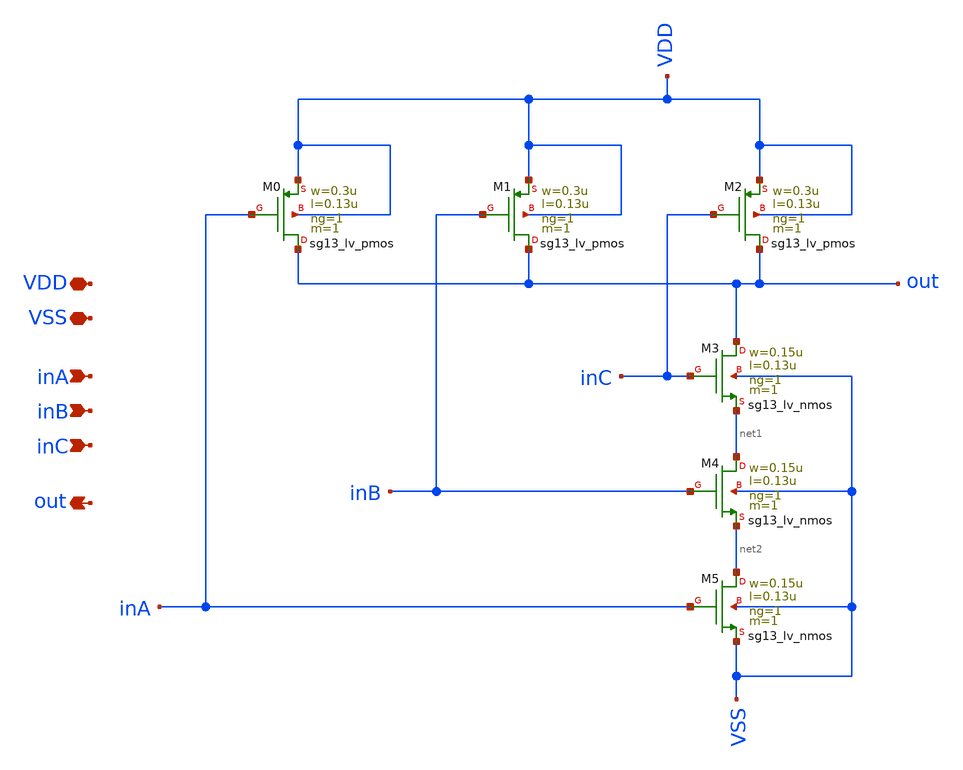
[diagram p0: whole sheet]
** sch_path: Team 2 Design/design_data/xschem/t2_nand3.sch
**.subckt t2_nand3 VSS inA inC out VDD inB
*.iopin VSS
*.ipin inA
*.ipin inC
*.opin out
*.iopin VDD
*.ipin inB
XM1 out inB VDD VDD sg13_lv_pmos w=0.3u l=0.13u ng=1 m=1 mm_ok=1
XM2 out inC VDD VDD sg13_lv_pmos w=0.3u l=0.13u ng=1 m=1 mm_ok=1
XM3 out inC net1 VSS sg13_lv_nmos w=0.15u l=0.13u ng=1 m=1 mm_ok=1
XM4 net1 inB net2 VSS sg13_lv_nmos w=0.15u l=0.13u ng=1 m=1 mm_ok=1
XM5 net2 inA VSS VSS sg13_lv_nmos w=0.15u l=0.13u ng=1 m=1 mm_ok=1
XM0 out inA VDD VDD sg13_lv_pmos w=0.3u l=0.13u ng=1 m=1 mm_ok=1
**.ends
.end
